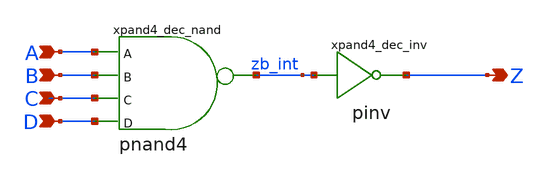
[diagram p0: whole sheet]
** sch_path: sram_4_16_scn4m/and4_dec.sch
**.subckt and4_dec A B C D Z
*.ipin A
*.ipin B
*.ipin C
*.ipin D
*.opin Z
xpand4_dec_nand A B C D zb_int vdd gnd pnand4
xpand4_dec_inv zb_int Z vdd gnd pinv
**.ends

* expanding   symbol:  pnand4.sym # of pins=5
** sym_path: sram_2_16_scn4m/pnand4.sym
** sch_path: sram_2_16_scn4m/pnand4.sch
.subckt pnand4 A B C D Z vdd gnd
*.ipin D
*.ipin C
*.ipin A
*.ipin B
*.opin Z
*.iopin vdd
*.iopin gnd
Mpnand4_nmos1 Z D net1 gnd n w=1.6u l=0.4u m=1
Mpnand3_pmos1 Z A vdd vdd p w=1.6u l=0.4u m=1
Mpnand4_pmos4 Z D vdd vdd p w=1.6u l=0.4u m=1
Mpnand4_nmos2 net1 C net2 gnd n w=1.6u l=0.4u m=1
Mpnand4_pmos3 Z C vdd vdd p w=1.6u l=0.4u m=1
Mpnand4_nmos3 net2 B net3 gnd n w=1.6u l=0.4u m=1
Mpnand4_pmos2 Z B vdd vdd p w=1.6u l=0.4u m=1
Mpnand4_nmos4 net3 A gnd gnd n w=1.6u l=0.4u m=1
.ends


* expanding   symbol:  pinv.sym # of pins=2
** sym_path: sram_4_16_scn4m/pinv.sym
** sch_path: sram_4_16_scn4m/pinv.sch
.subckt pinv A Z vdd gnd
*.ipin A
*.opin Z
XMpinv_nmos Z A gnd gnd sky130_fd_pr__nfet_01v8 L=0.4 W=0.8 nf=1 ad='int((nf+1)/2) * W/nf * 0.29' as='int((nf+2)/2) * W/nf * 0.29'
+ pd='2*int((nf+1)/2) * (W/nf + 0.29)' ps='2*int((nf+2)/2) * (W/nf + 0.29)' nrd='0.29 / W' nrs='0.29 / W'
+ sa=0 sb=0 sd=0 mult=1 m=1
XMp_inv_pmos Z A vdd vdd sky130_fd_pr__pfet_01v8 L=0.4 W=1.6 nf=1 ad='int((nf+1)/2) * W/nf * 0.29' as='int((nf+2)/2) * W/nf * 0.29'
+ pd='2*int((nf+1)/2) * (W/nf + 0.29)' ps='2*int((nf+2)/2) * (W/nf + 0.29)' nrd='0.29 / W' nrs='0.29 / W'
+ sa=0 sb=0 sd=0 mult=1 m=1
.ends

.end
